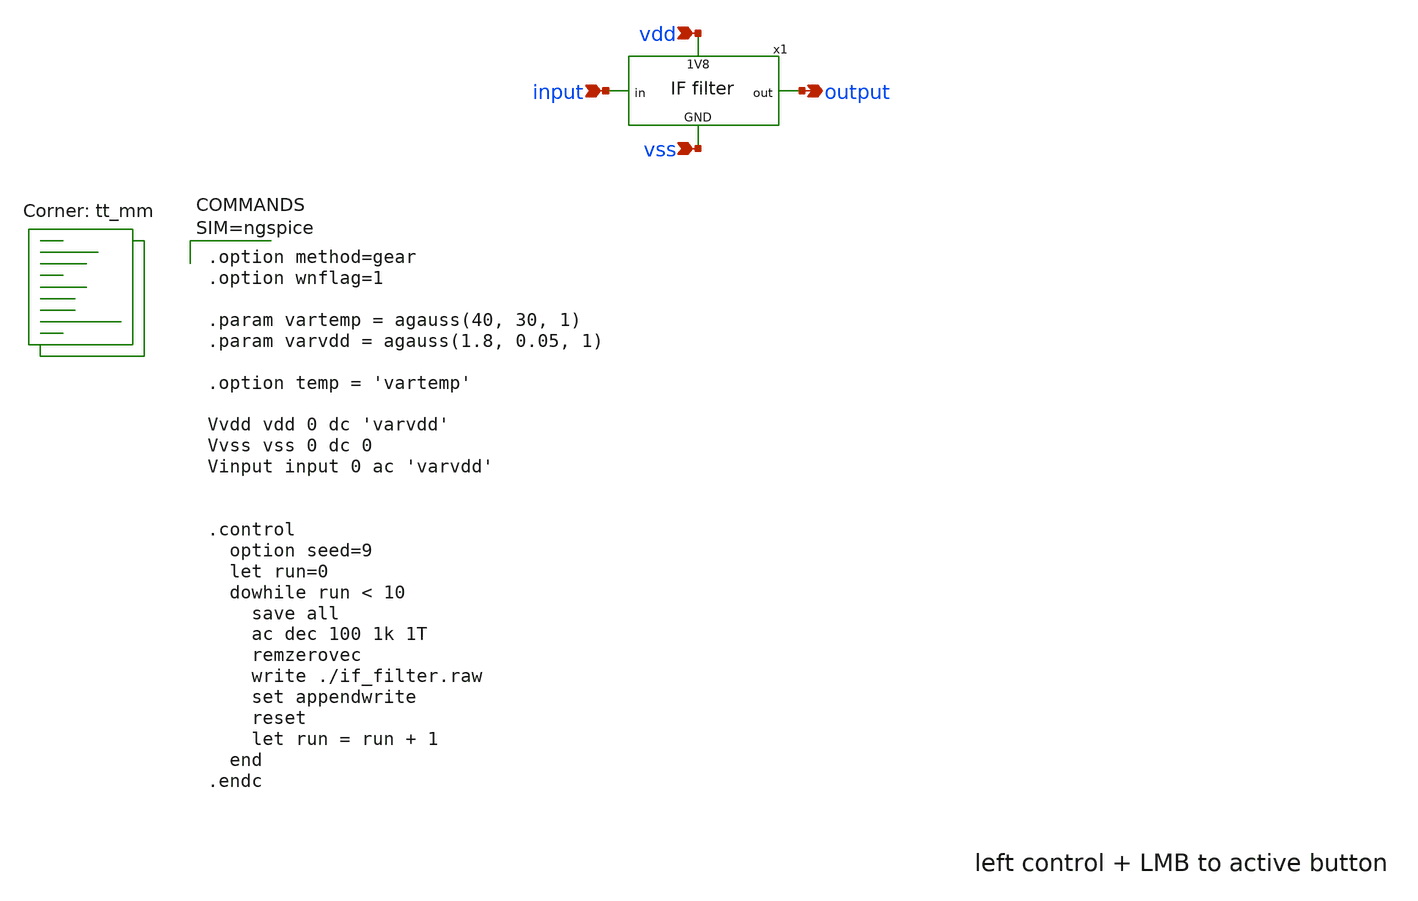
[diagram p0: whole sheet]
** sch_path: tests/if_filter.sch
**.subckt if_filter input output vdd vss
*.ipin input
*.opin output
*.ipin vdd
*.ipin vss
x1 vdd input output vss if_filter
**** begin user architecture code
.lib $::SKYWATER_MODELS/sky130.lib.spice tt_mm


.option method=gear
.option wnflag=1

.param vartemp = agauss(40, 30, 1)
.param varvdd = agauss(1.8, 0.05, 1)

.option temp = 'vartemp'

Vvdd vdd 0 dc 'varvdd'
Vvss vss 0 dc 0
Vinput input 0 ac 'varvdd'


.control
  option seed=9
  let run=0
  dowhile run < 10
    save all
    ac dec 100 1k 1T
    remzerovec
    write ./if_filter.raw
    set appendwrite
    reset
    let run = run + 1
  end
.endc


**** end user architecture code
**.ends

* expanding   symbol:  ./if_filter.sym # of pins=4
** sym_path: schematic/if_filter.sym
** sch_path: schematic/if_filter.sch
.subckt if_filter 1V8 in out GND
*.ipin in
*.opin out
*.ipin GND
*.ipin 1V8
* noconn 1V8
* noconn GND
R1 out in 0 m=1
.ends

.end
